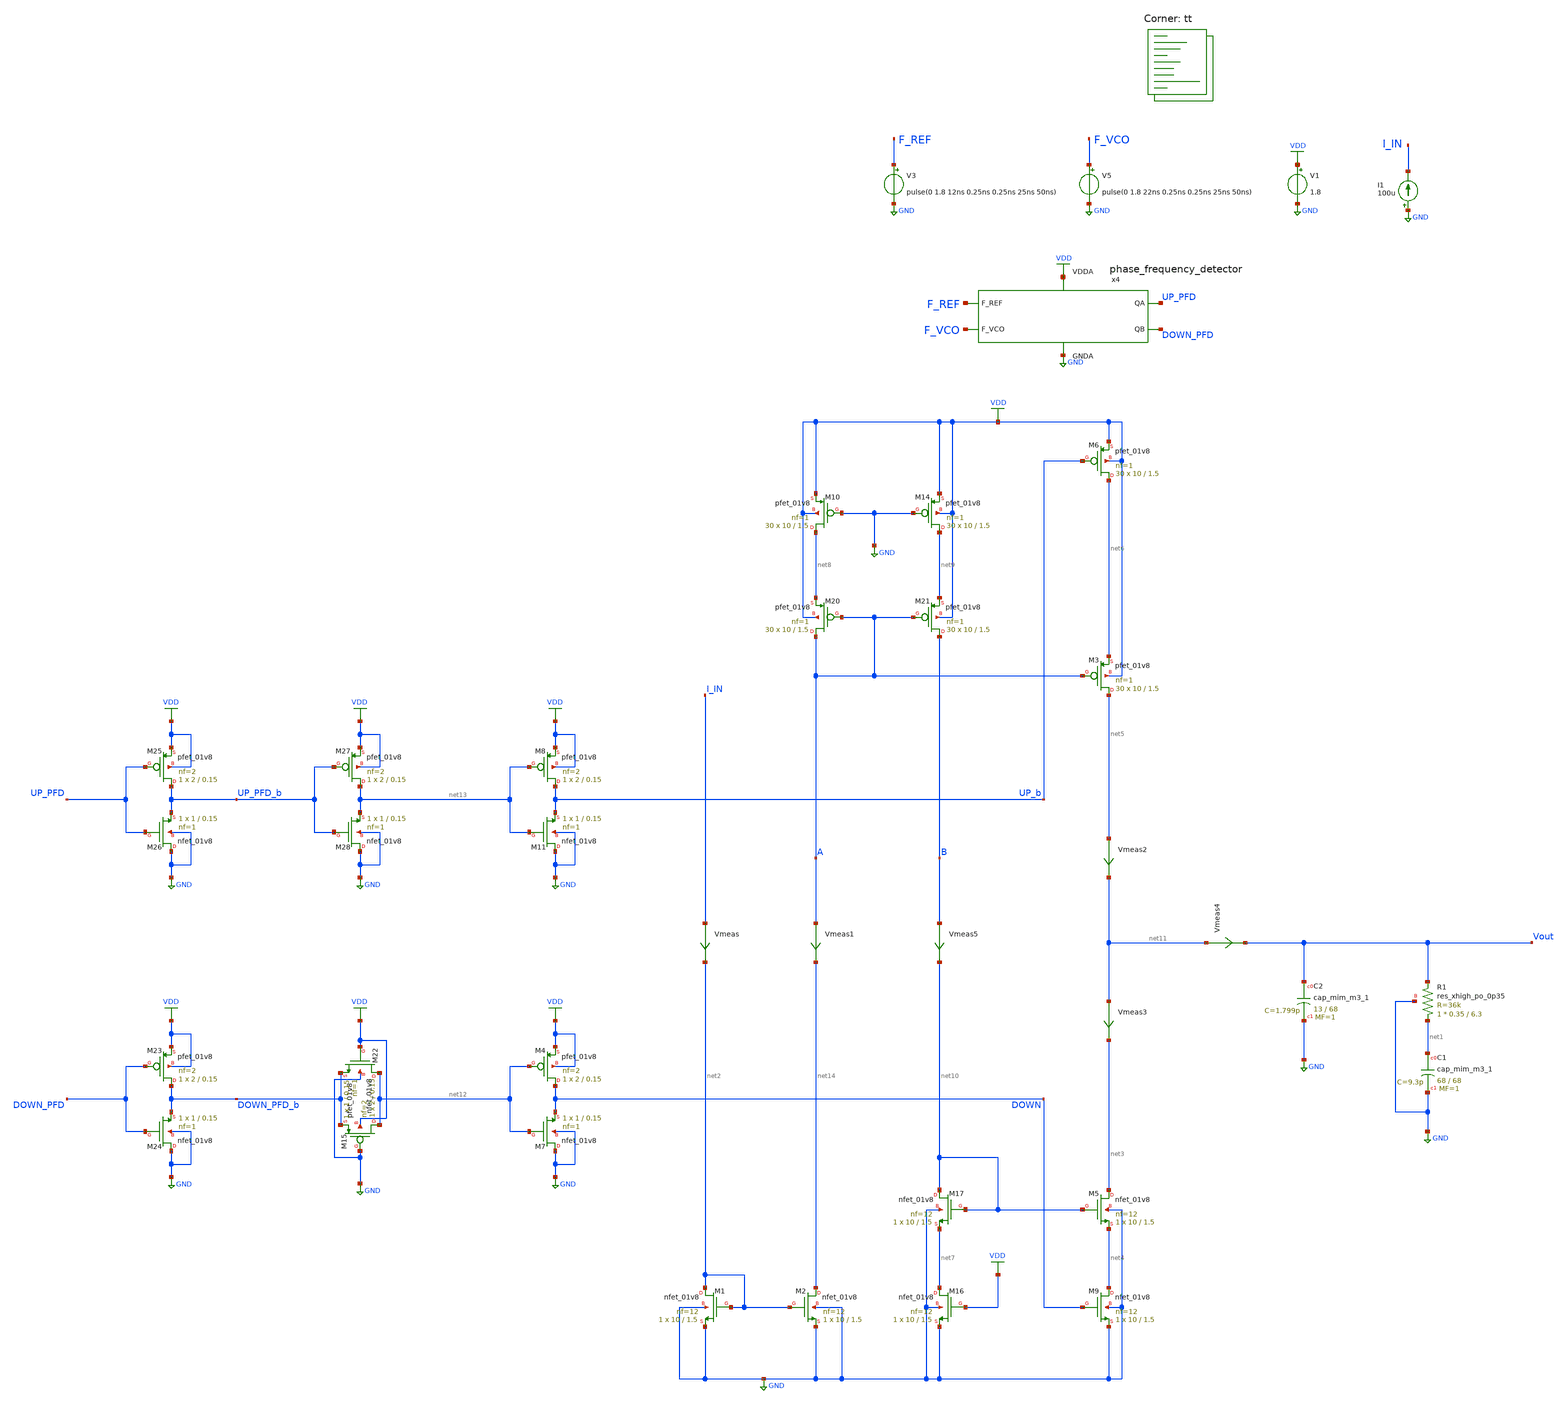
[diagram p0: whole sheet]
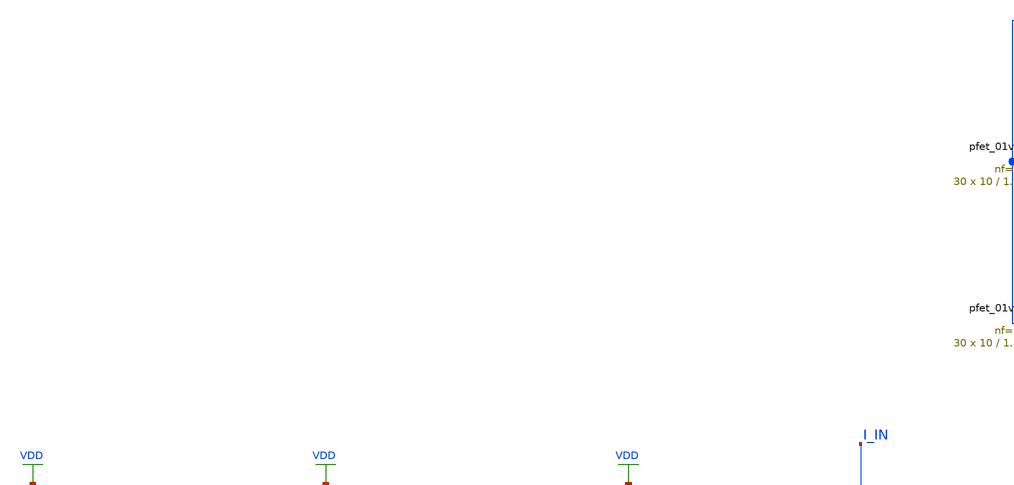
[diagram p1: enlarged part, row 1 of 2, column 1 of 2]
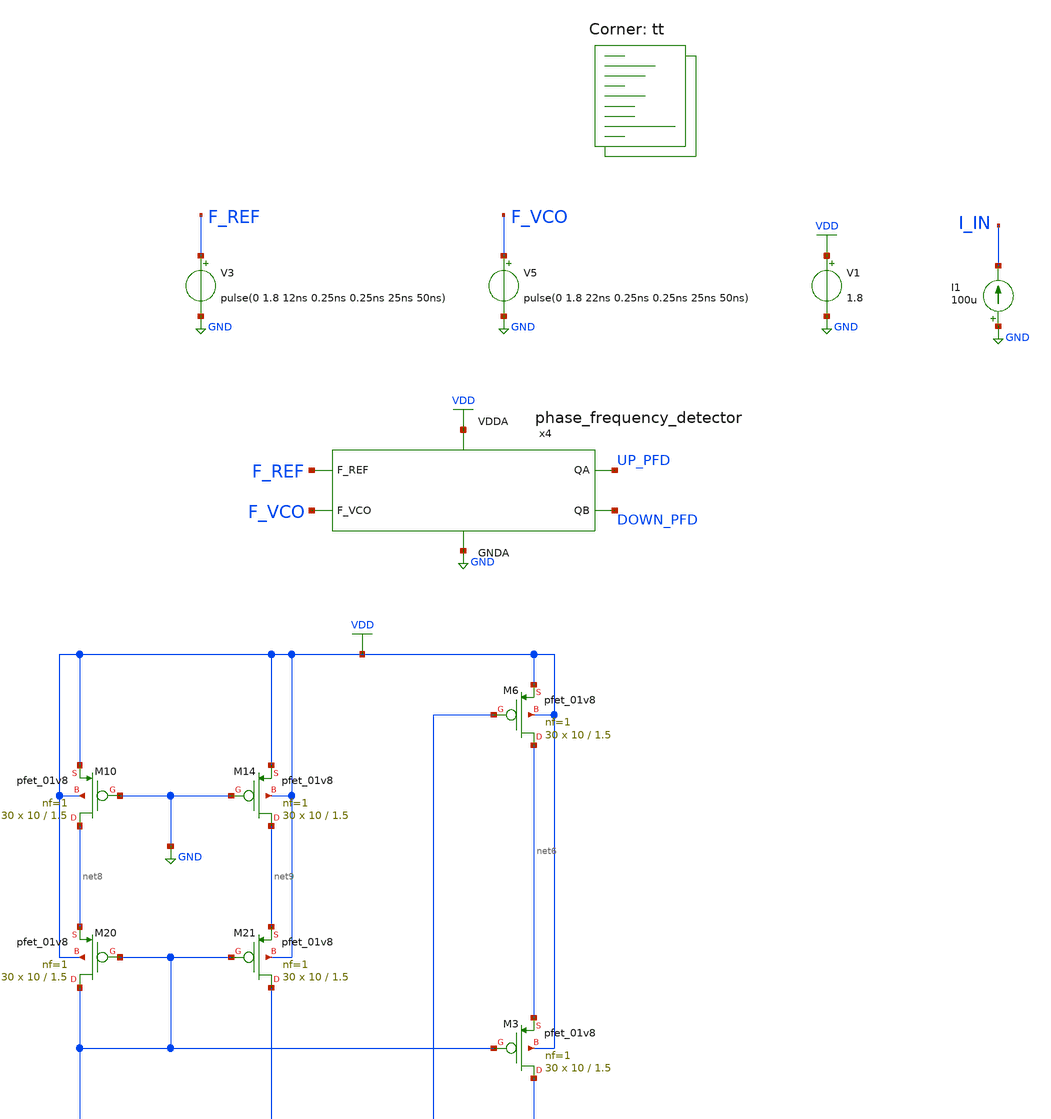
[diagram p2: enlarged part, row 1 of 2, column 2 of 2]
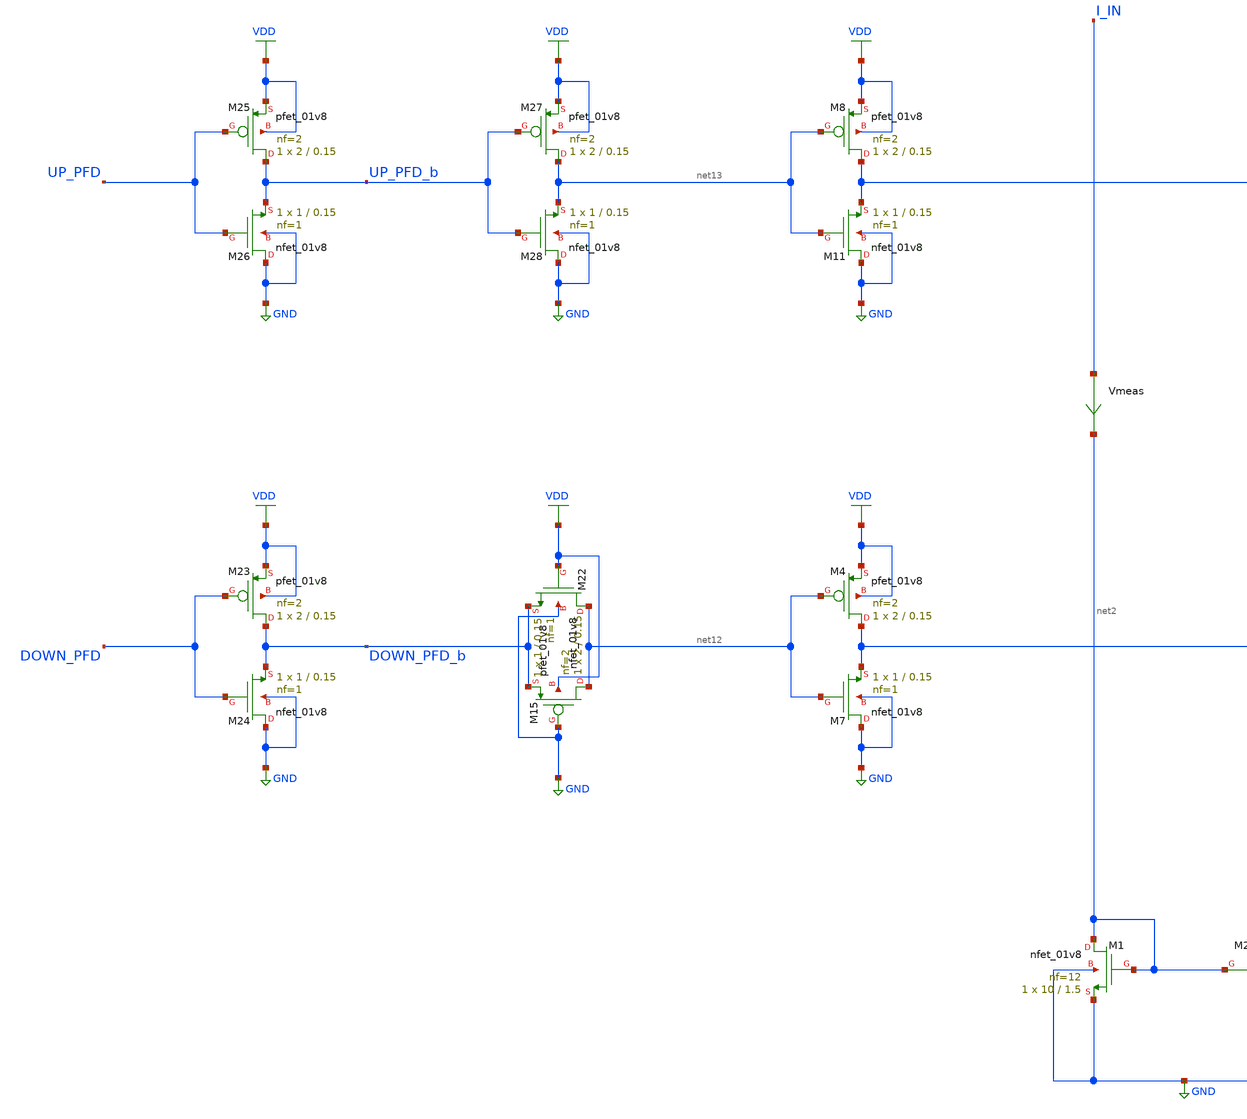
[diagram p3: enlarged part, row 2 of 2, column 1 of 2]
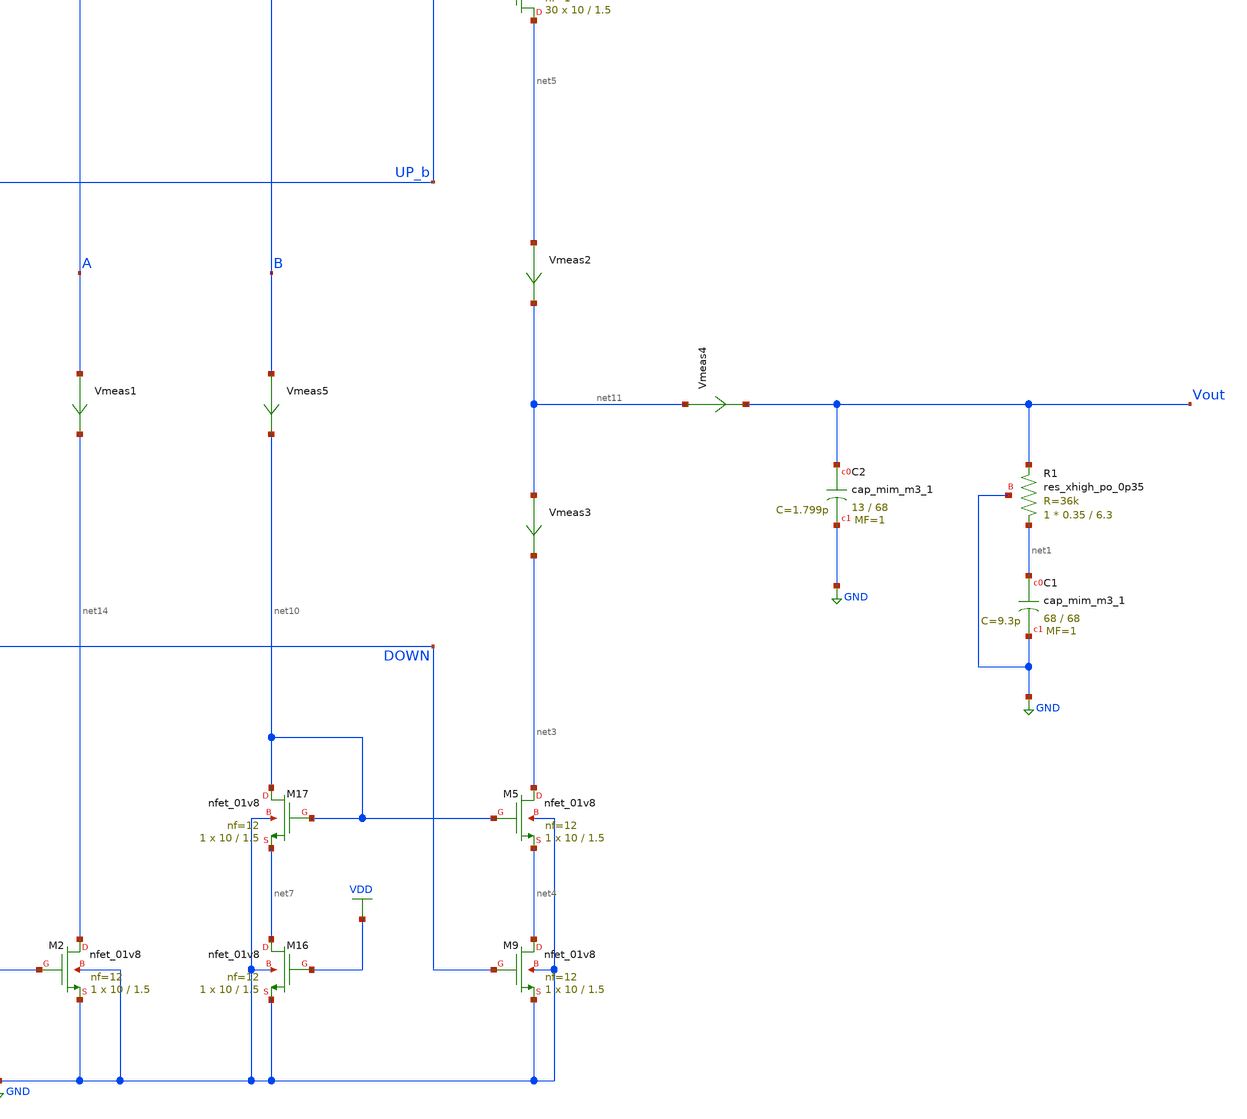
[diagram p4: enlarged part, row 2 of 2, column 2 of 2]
** sch_path: projects/pll/charge_pump/xschem_ngspice/pfd_charge_pump_3.sch
**.subckt pfd_charge_pump_3
V1 VDD GND 1.8
XC2 Vout GND sky130_fd_pr__cap_mim_m3_1 W=13 L=68 MF=1 m=1
XC1 net1 GND sky130_fd_pr__cap_mim_m3_1 W=68 L=68 MF=1 m=1
V3 F_REF GND pulse(0 1.8 12ns 0.25ns 0.25ns 25ns 50ns)
V5 F_VCO GND pulse(0 1.8 22ns 0.25ns 0.25ns 25ns 50ns)
x4 F_REF F_VCO VDD UP_PFD DOWN_PFD GND phase_frequency_detector
Vmeas4 net11 Vout 0
.save i(vmeas4)
XM1 net2 net2 GND GND sky130_fd_pr__nfet_01v8 L=1.5 W=10 nf=12 ad='int((nf+1)/2) * W/nf * 0.29' as='int((nf+2)/2) * W/nf * 0.29'
+ pd='2*int((nf+1)/2) * (W/nf + 0.29)' ps='2*int((nf+2)/2) * (W/nf + 0.29)' nrd='0.29 / W' nrs='0.29 / W'
+ sa=0 sb=0 sd=0 mult=1 m=1
XM2 net14 net2 GND GND sky130_fd_pr__nfet_01v8 L=1.5 W=10 nf=12 ad='int((nf+1)/2) * W/nf * 0.29' as='int((nf+2)/2) * W/nf * 0.29'
+ pd='2*int((nf+1)/2) * (W/nf + 0.29)' ps='2*int((nf+2)/2) * (W/nf + 0.29)' nrd='0.29 / W' nrs='0.29 / W'
+ sa=0 sb=0 sd=0 mult=1 m=1
Vmeas I_IN net2 0
.save i(vmeas)
XM6 net6 UP_b VDD VDD sky130_fd_pr__pfet_01v8 L=1.5 W=10 nf=1 ad='int((nf+1)/2) * W/nf * 0.29' as='int((nf+2)/2) * W/nf * 0.29'
+ pd='2*int((nf+1)/2) * (W/nf + 0.29)' ps='2*int((nf+2)/2) * (W/nf + 0.29)' nrd='0.29 / W' nrs='0.29 / W'
+ sa=0 sb=0 sd=0 mult=30 m=30
Vmeas2 net5 net11 0
.save i(vmeas2)
Vmeas3 net11 net3 0
.save i(vmeas3)
XM9 net4 DOWN GND GND sky130_fd_pr__nfet_01v8 L=1.5 W=10 nf=12 ad='int((nf+1)/2) * W/nf * 0.29' as='int((nf+2)/2) * W/nf * 0.29'
+ pd='2*int((nf+1)/2) * (W/nf + 0.29)' ps='2*int((nf+2)/2) * (W/nf + 0.29)' nrd='0.29 / W' nrs='0.29 / W'
+ sa=0 sb=0 sd=0 mult=1 m=1
XM3 net5 A net6 VDD sky130_fd_pr__pfet_01v8 L=1.5 W=10 nf=1 ad='int((nf+1)/2) * W/nf * 0.29' as='int((nf+2)/2) * W/nf * 0.29'
+ pd='2*int((nf+1)/2) * (W/nf + 0.29)' ps='2*int((nf+2)/2) * (W/nf + 0.29)' nrd='0.29 / W' nrs='0.29 / W'
+ sa=0 sb=0 sd=0 mult=30 m=30
XM5 net3 net10 net4 GND sky130_fd_pr__nfet_01v8 L=1.5 W=10 nf=12 ad='int((nf+1)/2) * W/nf * 0.29' as='int((nf+2)/2) * W/nf * 0.29'
+ pd='2*int((nf+1)/2) * (W/nf + 0.29)' ps='2*int((nf+2)/2) * (W/nf + 0.29)' nrd='0.29 / W' nrs='0.29 / W'
+ sa=0 sb=0 sd=0 mult=1 m=1
XM10 net8 GND VDD VDD sky130_fd_pr__pfet_01v8 L=1.5 W=10 nf=1 ad='int((nf+1)/2) * W/nf * 0.29' as='int((nf+2)/2) * W/nf * 0.29'
+ pd='2*int((nf+1)/2) * (W/nf + 0.29)' ps='2*int((nf+2)/2) * (W/nf + 0.29)' nrd='0.29 / W' nrs='0.29 / W'
+ sa=0 sb=0 sd=0 mult=30 m=30
XM14 net9 GND VDD VDD sky130_fd_pr__pfet_01v8 L=1.5 W=10 nf=1 ad='int((nf+1)/2) * W/nf * 0.29' as='int((nf+2)/2) * W/nf * 0.29'
+ pd='2*int((nf+1)/2) * (W/nf + 0.29)' ps='2*int((nf+2)/2) * (W/nf + 0.29)' nrd='0.29 / W' nrs='0.29 / W'
+ sa=0 sb=0 sd=0 mult=30 m=30
XM16 net7 VDD GND GND sky130_fd_pr__nfet_01v8 L=1.5 W=10 nf=12 ad='int((nf+1)/2) * W/nf * 0.29' as='int((nf+2)/2) * W/nf * 0.29'
+ pd='2*int((nf+1)/2) * (W/nf + 0.29)' ps='2*int((nf+2)/2) * (W/nf + 0.29)' nrd='0.29 / W' nrs='0.29 / W'
+ sa=0 sb=0 sd=0 mult=1 m=1
XM17 net10 net10 net7 GND sky130_fd_pr__nfet_01v8 L=1.5 W=10 nf=12 ad='int((nf+1)/2) * W/nf * 0.29' as='int((nf+2)/2) * W/nf * 0.29'
+ pd='2*int((nf+1)/2) * (W/nf + 0.29)' ps='2*int((nf+2)/2) * (W/nf + 0.29)' nrd='0.29 / W' nrs='0.29 / W'
+ sa=0 sb=0 sd=0 mult=1 m=1
XM20 A A net8 VDD sky130_fd_pr__pfet_01v8 L=1.5 W=10 nf=1 ad='int((nf+1)/2) * W/nf * 0.29' as='int((nf+2)/2) * W/nf * 0.29'
+ pd='2*int((nf+1)/2) * (W/nf + 0.29)' ps='2*int((nf+2)/2) * (W/nf + 0.29)' nrd='0.29 / W' nrs='0.29 / W'
+ sa=0 sb=0 sd=0 mult=30 m=30
XM21 B A net9 VDD sky130_fd_pr__pfet_01v8 L=1.5 W=10 nf=1 ad='int((nf+1)/2) * W/nf * 0.29' as='int((nf+2)/2) * W/nf * 0.29'
+ pd='2*int((nf+1)/2) * (W/nf + 0.29)' ps='2*int((nf+2)/2) * (W/nf + 0.29)' nrd='0.29 / W' nrs='0.29 / W'
+ sa=0 sb=0 sd=0 mult=30 m=30
Vmeas1 A net14 0
.save i(vmeas1)
Vmeas5 B net10 0
.save i(vmeas5)
XM15 net12 GND DOWN_PFD_b VDD sky130_fd_pr__pfet_01v8 L=0.15 W=2 nf=2 ad='int((nf+1)/2) * W/nf * 0.29'
+ as='int((nf+2)/2) * W/nf * 0.29' pd='2*int((nf+1)/2) * (W/nf + 0.29)' ps='2*int((nf+2)/2) * (W/nf + 0.29)'
+ nrd='0.29 / W' nrs='0.29 / W' sa=0 sb=0 sd=0 mult=1 m=1
XM22 net12 VDD DOWN_PFD_b GND sky130_fd_pr__nfet_01v8 L=0.15 W=1 nf=1 ad='int((nf+1)/2) * W/nf * 0.29'
+ as='int((nf+2)/2) * W/nf * 0.29' pd='2*int((nf+1)/2) * (W/nf + 0.29)' ps='2*int((nf+2)/2) * (W/nf + 0.29)'
+ nrd='0.29 / W' nrs='0.29 / W' sa=0 sb=0 sd=0 mult=1 m=1
XM23 DOWN_PFD_b DOWN_PFD VDD VDD sky130_fd_pr__pfet_01v8 L=0.15 W=2 nf=2 ad='int((nf+1)/2) * W/nf * 0.29'
+ as='int((nf+2)/2) * W/nf * 0.29' pd='2*int((nf+1)/2) * (W/nf + 0.29)' ps='2*int((nf+2)/2) * (W/nf + 0.29)'
+ nrd='0.29 / W' nrs='0.29 / W' sa=0 sb=0 sd=0 mult=1 m=1
XM24 GND DOWN_PFD DOWN_PFD_b GND sky130_fd_pr__nfet_01v8 L=0.15 W=1 nf=1 ad='int((nf+1)/2) * W/nf * 0.29'
+ as='int((nf+2)/2) * W/nf * 0.29' pd='2*int((nf+1)/2) * (W/nf + 0.29)' ps='2*int((nf+2)/2) * (W/nf + 0.29)'
+ nrd='0.29 / W' nrs='0.29 / W' sa=0 sb=0 sd=0 mult=1 m=1
XM25 UP_PFD_b UP_PFD VDD VDD sky130_fd_pr__pfet_01v8 L=0.15 W=2 nf=2 ad='int((nf+1)/2) * W/nf * 0.29'
+ as='int((nf+2)/2) * W/nf * 0.29' pd='2*int((nf+1)/2) * (W/nf + 0.29)' ps='2*int((nf+2)/2) * (W/nf + 0.29)'
+ nrd='0.29 / W' nrs='0.29 / W' sa=0 sb=0 sd=0 mult=1 m=1
XM26 GND UP_PFD UP_PFD_b GND sky130_fd_pr__nfet_01v8 L=0.15 W=1 nf=1 ad='int((nf+1)/2) * W/nf * 0.29'
+ as='int((nf+2)/2) * W/nf * 0.29' pd='2*int((nf+1)/2) * (W/nf + 0.29)' ps='2*int((nf+2)/2) * (W/nf + 0.29)'
+ nrd='0.29 / W' nrs='0.29 / W' sa=0 sb=0 sd=0 mult=1 m=1
XM27 net13 UP_PFD_b VDD VDD sky130_fd_pr__pfet_01v8 L=0.15 W=2 nf=2 ad='int((nf+1)/2) * W/nf * 0.29'
+ as='int((nf+2)/2) * W/nf * 0.29' pd='2*int((nf+1)/2) * (W/nf + 0.29)' ps='2*int((nf+2)/2) * (W/nf + 0.29)'
+ nrd='0.29 / W' nrs='0.29 / W' sa=0 sb=0 sd=0 mult=1 m=1
XM28 GND UP_PFD_b net13 GND sky130_fd_pr__nfet_01v8 L=0.15 W=1 nf=1 ad='int((nf+1)/2) * W/nf * 0.29'
+ as='int((nf+2)/2) * W/nf * 0.29' pd='2*int((nf+1)/2) * (W/nf + 0.29)' ps='2*int((nf+2)/2) * (W/nf + 0.29)'
+ nrd='0.29 / W' nrs='0.29 / W' sa=0 sb=0 sd=0 mult=1 m=1
XR1 net1 Vout GND sky130_fd_pr__res_xhigh_po_0p35 L=6.3 mult=1 m=1
I1 GND I_IN 100u
XM4 DOWN net12 VDD VDD sky130_fd_pr__pfet_01v8 L=0.15 W=2 nf=2 ad='int((nf+1)/2) * W/nf * 0.29' as='int((nf+2)/2) * W/nf * 0.29'
+ pd='2*int((nf+1)/2) * (W/nf + 0.29)' ps='2*int((nf+2)/2) * (W/nf + 0.29)' nrd='0.29 / W' nrs='0.29 / W'
+ sa=0 sb=0 sd=0 mult=1 m=1
XM7 GND net12 DOWN GND sky130_fd_pr__nfet_01v8 L=0.15 W=1 nf=1 ad='int((nf+1)/2) * W/nf * 0.29' as='int((nf+2)/2) * W/nf * 0.29'
+ pd='2*int((nf+1)/2) * (W/nf + 0.29)' ps='2*int((nf+2)/2) * (W/nf + 0.29)' nrd='0.29 / W' nrs='0.29 / W'
+ sa=0 sb=0 sd=0 mult=1 m=1
XM8 UP_b net13 VDD VDD sky130_fd_pr__pfet_01v8 L=0.15 W=2 nf=2 ad='int((nf+1)/2) * W/nf * 0.29' as='int((nf+2)/2) * W/nf * 0.29'
+ pd='2*int((nf+1)/2) * (W/nf + 0.29)' ps='2*int((nf+2)/2) * (W/nf + 0.29)' nrd='0.29 / W' nrs='0.29 / W'
+ sa=0 sb=0 sd=0 mult=1 m=1
XM11 GND net13 UP_b GND sky130_fd_pr__nfet_01v8 L=0.15 W=1 nf=1 ad='int((nf+1)/2) * W/nf * 0.29' as='int((nf+2)/2) * W/nf * 0.29'
+ pd='2*int((nf+1)/2) * (W/nf + 0.29)' ps='2*int((nf+2)/2) * (W/nf + 0.29)' nrd='0.29 / W' nrs='0.29 / W'
+ sa=0 sb=0 sd=0 mult=1 m=1
**** begin user architecture code
.lib $::SKYWATER_MODELS/sky130.lib.spice tt



.include /foss/pdks/sky130A/libs.ref/sky130_fd_sc_hd/spice/sky130_fd_sc_hd.spice

.option method=gear trtol1
.option wnflag=1
* .option savecurrents

* .temp = 75

.ic v(vout) = 0


.control
  * save v(up_pfd) v(down_pfd) v(up_pfd_b) v(down_pfd_b) v(up) v(up_b) v(down) v(down_b) v(x)
+ v(vout) v(up_input) v(down_input)
  save all

  tran 0.1ns 1us
  * dc v2 0 1.8 0.01
  remzerovec
  write pfd_charge_pump_3.raw
  * wrdata /foss/designs/my_design/projects/pll/pfd/xschem_ngspice/charge_pump3_QA.txt v(osc)
  set appendwrite

.endc






**** end user architecture code
**.ends

* expanding   symbol:
*+  /foss/designs/my_design/projects/pll/pfd/xschem_ngspice/phase_frequency_detector.sym # of pins=6
** sym_path: projects/pll/pfd/xschem_ngspice/phase_frequency_detector.sym
** sch_path: projects/pll/pfd/xschem_ngspice/phase_frequency_detector.sch
.subckt phase_frequency_detector F_REF F_VCO VDDA QA QB GNDA
*.ipin F_REF
*.opin QA
*.ipin F_VCO
*.opin QB
*.ipin VDDA
*.ipin GNDA
x1 F_REF QA GNDA GNDA VDDA VDDA QA_b sky130_fd_sc_hd__nor2_1
x2 QA_b E GNDA GNDA VDDA VDDA QA sky130_fd_sc_hd__nor2_1
x3 QA_b E_b GNDA GNDA VDDA VDDA E sky130_fd_sc_hd__nor2_1
x4 E Reset GNDA GNDA VDDA VDDA E_b sky130_fd_sc_hd__nor2_1
x5 F_VCO QB GNDA GNDA VDDA VDDA QB_b sky130_fd_sc_hd__nor2_1
x6 QB_b F GNDA GNDA VDDA VDDA QB sky130_fd_sc_hd__nor2_1
x7 QB_b F_b GNDA GNDA VDDA VDDA F sky130_fd_sc_hd__nor2_1
x8 F Reset GNDA GNDA VDDA VDDA F_b sky130_fd_sc_hd__nor2_1
x9 QA QB GNDA GNDA VDDA VDDA before_Reset sky130_fd_sc_hd__nand2_1
x10 before_Reset GNDA GNDA VDDA VDDA net1 sky130_fd_sc_hd__inv_1
x11 net1 GNDA GNDA VDDA VDDA net2 sky130_fd_sc_hd__inv_1
x12 net2 GNDA GNDA VDDA VDDA net3 sky130_fd_sc_hd__inv_1
x13 net3 GNDA GNDA VDDA VDDA net4 sky130_fd_sc_hd__inv_1
x14 net4 GNDA GNDA VDDA VDDA Reset sky130_fd_sc_hd__inv_1
.ends

.GLOBAL GND
.GLOBAL VDD
.end
